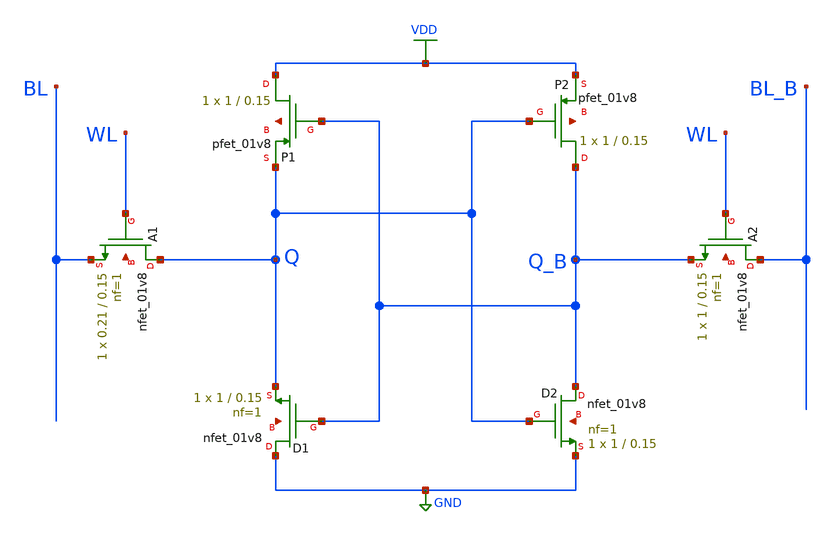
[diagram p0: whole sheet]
** sch_path: xschem/6T_SRAM.sch
**.subckt 6T_SRAM
XA1 Q WL BL net1 sky130_fd_pr__nfet_01v8 L=0.15 W=0.21 nf=1 ad='int((nf+1)/2) * W/nf * 0.29' as='int((nf+2)/2) * W/nf * 0.29'
+ pd='2*int((nf+1)/2) * (W/nf + 0.29)' ps='2*int((nf+2)/2) * (W/nf + 0.29)' nrd='0.29 / W' nrs='0.29 / W'
+ sa=0 sb=0 sd=0 mult=1 m=1
XA2 BL_B WL Q_B net2 sky130_fd_pr__nfet_01v8 L=0.15 W=1 nf=1 ad='int((nf+1)/2) * W/nf * 0.29' as='int((nf+2)/2) * W/nf * 0.29'
+ pd='2*int((nf+1)/2) * (W/nf + 0.29)' ps='2*int((nf+2)/2) * (W/nf + 0.29)' nrd='0.29 / W' nrs='0.29 / W'
+ sa=0 sb=0 sd=0 mult=1 m=1
XD1 GND Q_B Q net3 sky130_fd_pr__nfet_01v8 L=0.15 W=1 nf=1 ad='int((nf+1)/2) * W/nf * 0.29' as='int((nf+2)/2) * W/nf * 0.29'
+ pd='2*int((nf+1)/2) * (W/nf + 0.29)' ps='2*int((nf+2)/2) * (W/nf + 0.29)' nrd='0.29 / W' nrs='0.29 / W'
+ sa=0 sb=0 sd=0 mult=1 m=1
XD2 Q_B Q GND net4 sky130_fd_pr__nfet_01v8 L=0.15 W=1 nf=1 ad='int((nf+1)/2) * W/nf * 0.29' as='int((nf+2)/2) * W/nf * 0.29'
+ pd='2*int((nf+1)/2) * (W/nf + 0.29)' ps='2*int((nf+2)/2) * (W/nf + 0.29)' nrd='0.29 / W' nrs='0.29 / W'
+ sa=0 sb=0 sd=0 mult=1 m=1
XP1 VDD Q_B Q net5 sky130_fd_pr__pfet_01v8 W=1 L=0.15 ad='int((nf+1)/2) * W/nf * 0.29' pd='2*int((nf+1)/2) * (W/nf + 0.29)'
+ as='int((nf+2)/2) * W/nf * 0.29' ps='2*int((nf+2)/2) * (W/nf + 0.29)' nrd='0.29 / W' nrs='0.29 / W' sa=0
+ sb=0 sd=0 nf=1 mult=1
XP2 Q_B Q VDD net6 sky130_fd_pr__pfet_01v8 W=1 L=0.15 ad='int((nf+1)/2) * W/nf * 0.29' pd='2*int((nf+1)/2) * (W/nf + 0.29)'
+ as='int((nf+2)/2) * W/nf * 0.29' ps='2*int((nf+2)/2) * (W/nf + 0.29)' nrd='0.29 / W' nrs='0.29 / W' sa=0
+ sb=0 sd=0 nf=1 mult=1
**.ends
.GLOBAL GND
.GLOBAL VDD
.end
